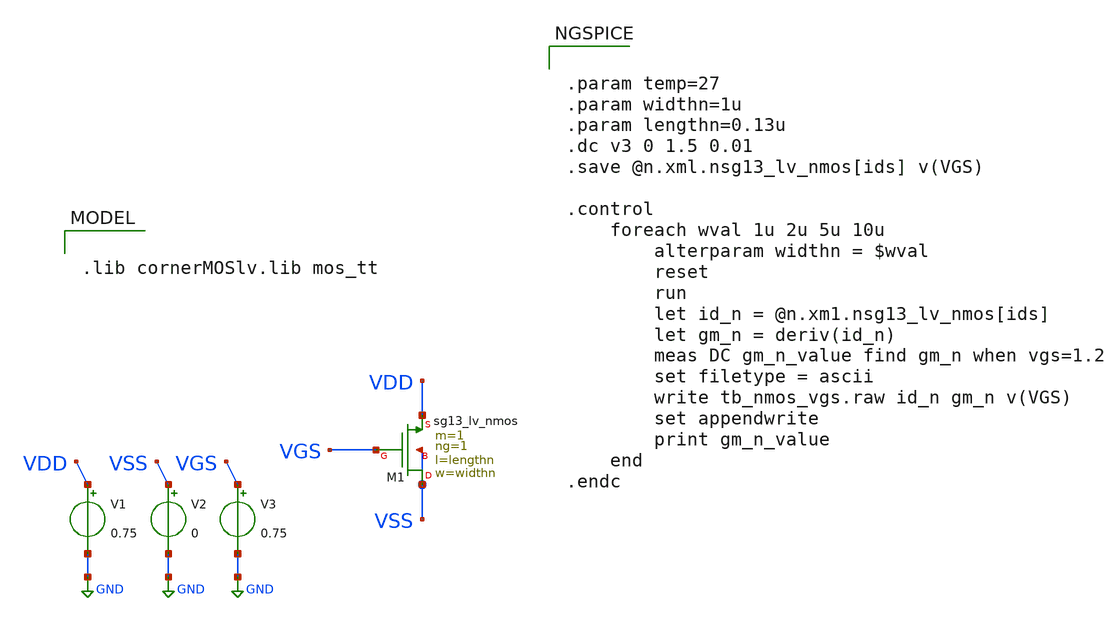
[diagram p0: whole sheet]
** sch_path: designs/1iee34/tb_nmos_vgs.sch
**.subckt tb_nmos_vgs
V1 VDD GND 0.75
V2 VSS GND 0
V3 VGS GND 0.75
XM1 VSS VGS VDD VSS sg13_lv_nmos w=widthn l=lengthn ng=1 m=1 mm_ok=1
**** begin user architecture code

.lib cornerMOSlv.lib mos_tt



.param temp=27
.param widthn=1u
.param lengthn=0.13u
.dc v3 0 1.5 0.01
.save @n.xml.nsg13_lv_nmos[ids] v(VGS)

.control
	foreach wval 1u 2u 5u 10u
		alterparam widthn = $wval
		reset
		run
		let id_n = @n.xm1.nsg13_lv_nmos[ids]
		let gm_n = deriv(id_n)
		meas DC gm_n_value find gm_n when vgs=1.2
		set filetype = ascii
		write tb_nmos_vgs.raw id_n gm_n v(VGS)
		set appendwrite
		print gm_n_value
	end
.endc


**** end user architecture code
**.ends
.GLOBAL GND
.end
